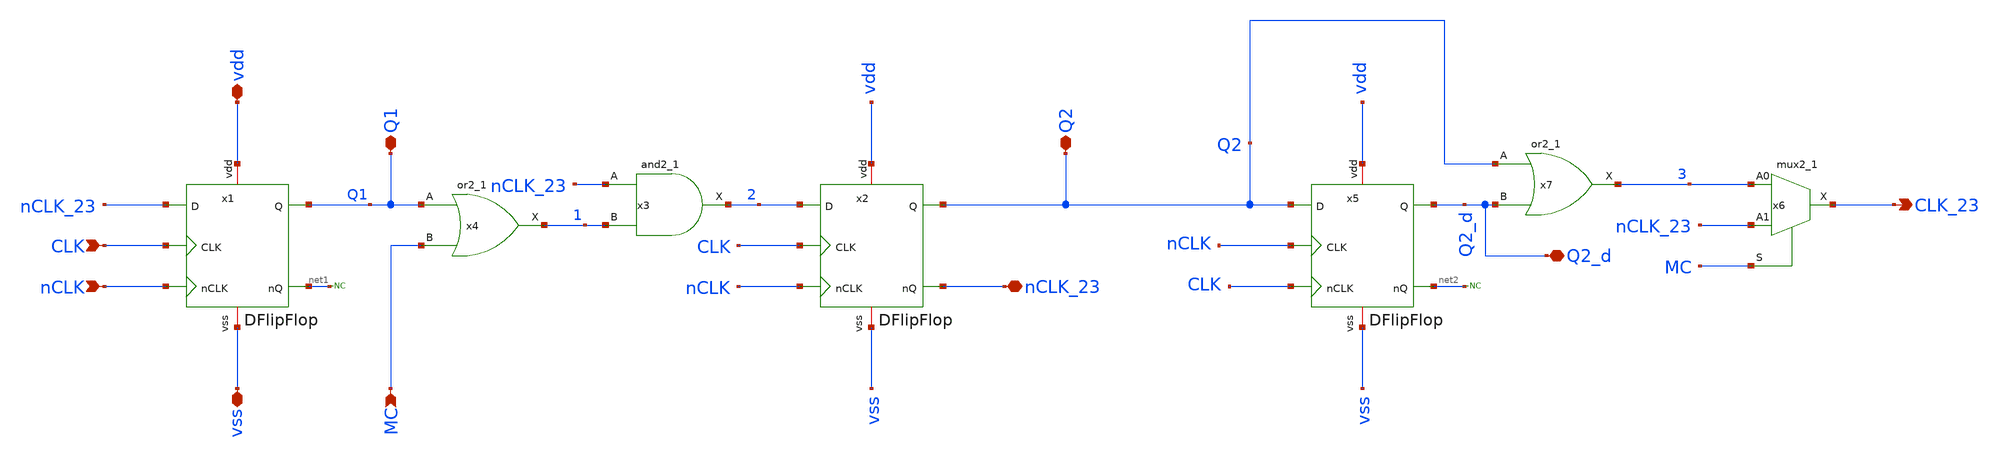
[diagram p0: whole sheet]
** sch_path: xschem/prescaler_23.sch
**.subckt prescaler_23 vdd CLK nCLK MC vss CLK_23 nCLK_23 Q1 Q2 Q2_d
*.iopin vdd
*.ipin CLK
*.ipin nCLK
*.ipin MC
*.iopin vss
*.opin CLK_23
*.iopin nCLK_23
*.iopin Q1
*.iopin Q2
*.iopin Q2_d
x3 nCLK_23 1 vss vss vdd vdd 2 sky130_fd_sc_hs__and2_1
x4 Q1 MC vss vss vdd vdd 1 sky130_fd_sc_hs__or2_1
x6 3 nCLK_23 MC vss vss vdd vdd CLK_23 sky130_fd_sc_hs__mux2_1
x7 Q2 Q2_d vss vss vdd vdd 3 sky130_fd_sc_hs__or2_1
x1 vdd Q1 net1 vss nCLK_23 CLK nCLK DFlipFlop
x2 vdd Q2 nCLK_23 vss 2 CLK nCLK DFlipFlop
x5 vdd Q2_d net2 vss Q2 nCLK CLK DFlipFlop
* noconn #net1
* noconn #net2
**.ends
.end
